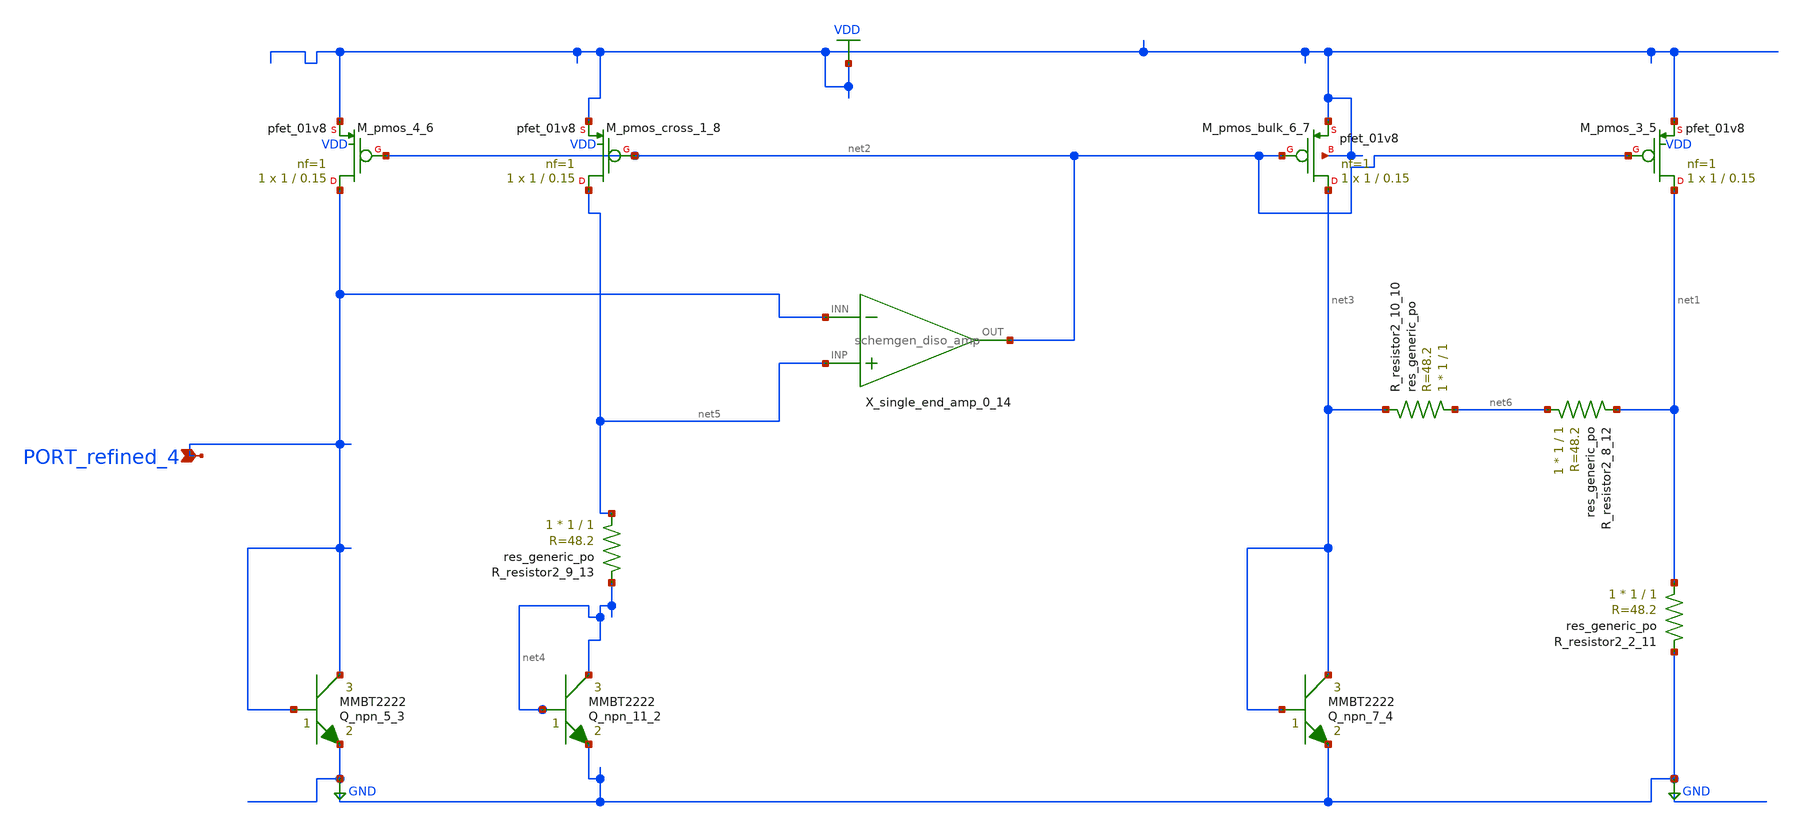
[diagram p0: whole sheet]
** sch_path: schematics/Image2Net/108.sch
**.subckt 108 PORT_refined_4
*.ipin PORT_refined_4
Q_npn_11_2 net4 net4 GND MMBT2222 area=1 m=1
Q_npn_5_3 PORT_refined_4 PORT_refined_4 GND MMBT2222 area=1 m=1
Q_npn_7_4 net3 net3 GND MMBT2222 area=1 m=1
XM_pmos_3_5 net1 net2 VDD VDD sky130_fd_pr__pfet_01v8 L=0.15 W=1 nf=1 ad='int((1 + 1)/2) * 1 / 1 * 0.29'
+ as='int((1 + 2)/2) * 1 / 1 * 0.29' pd='2*int((1 + 1)/2) * (1 / 1 + 0.29)' ps='2*int((1 + 2)/2) * (1 / 1 + 0.29)'
+ nrd='0.29 / 1 ' nrs='0.29 / 1 ' sa=0 sb=0 sd=0 mult=1 m=1
XM_pmos_4_6 PORT_refined_4 net2 VDD VDD sky130_fd_pr__pfet_01v8 L=0.15 W=1 nf=1 ad='int((1 + 1)/2) * 1 / 1 * 0.29'
+ as='int((1 + 2)/2) * 1 / 1 * 0.29' pd='2*int((1 + 1)/2) * (1 / 1 + 0.29)' ps='2*int((1 + 2)/2) * (1 / 1 + 0.29)'
+ nrd='0.29 / 1 ' nrs='0.29 / 1 ' sa=0 sb=0 sd=0 mult=1 m=1
XM_pmos_bulk_6_7 net3 net2 VDD VDD sky130_fd_pr__pfet_01v8 L=0.15 W=1 nf=1 ad='int((1 + 1)/2) * 1 / 1 * 0.29'
+ as='int((1 + 2)/2) * 1 / 1 * 0.29' pd='2*int((1 + 1)/2) * (1 / 1 + 0.29)' ps='2*int((1 + 2)/2) * (1 / 1 + 0.29)'
+ nrd='0.29 / 1 ' nrs='0.29 / 1 ' sa=0 sb=0 sd=0 mult=1 m=1
XM_pmos_cross_1_8 net5 net2 VDD VDD sky130_fd_pr__pfet_01v8 L=0.15 W=1 nf=1 ad='int((1 + 1)/2) * 1 / 1 * 0.29'
+ as='int((1 + 2)/2) * 1 / 1 * 0.29' pd='2*int((1 + 1)/2) * (1 / 1 + 0.29)' ps='2*int((1 + 2)/2) * (1 / 1 + 0.29)'
+ nrd='0.29 / 1 ' nrs='0.29 / 1 ' sa=0 sb=0 sd=0 mult=1 m=1
XR_resistor2_10_10 net6 net3 sky130_fd_pr__res_generic_po W=1 L=1 m=1
XR_resistor2_2_11 net1 GND sky130_fd_pr__res_generic_po W=1 L=1 m=1
XR_resistor2_8_12 net6 net1 sky130_fd_pr__res_generic_po W=1 L=1 m=1
XR_resistor2_9_13 net5 net4 sky130_fd_pr__res_generic_po W=1 L=1 m=1
X_single_end_amp_0_14 net5 PORT_refined_4 net2 schemgen_diso_amp
**.ends

* expanding   symbol:  schemgen_diso_amp.sym # of pins=3
** sym_path: symbols/schemgen_diso_amp.sym
.subckt schemgen_diso_amp INP INN OUT
* SchemGen ideal op-amp: Vout = 1e5 * (V(INP) - V(INN))
E1 OUT 0 INP INN 1e5
.ends schemgen_diso_amp
.GLOBAL GND
.GLOBAL VDD
.end
